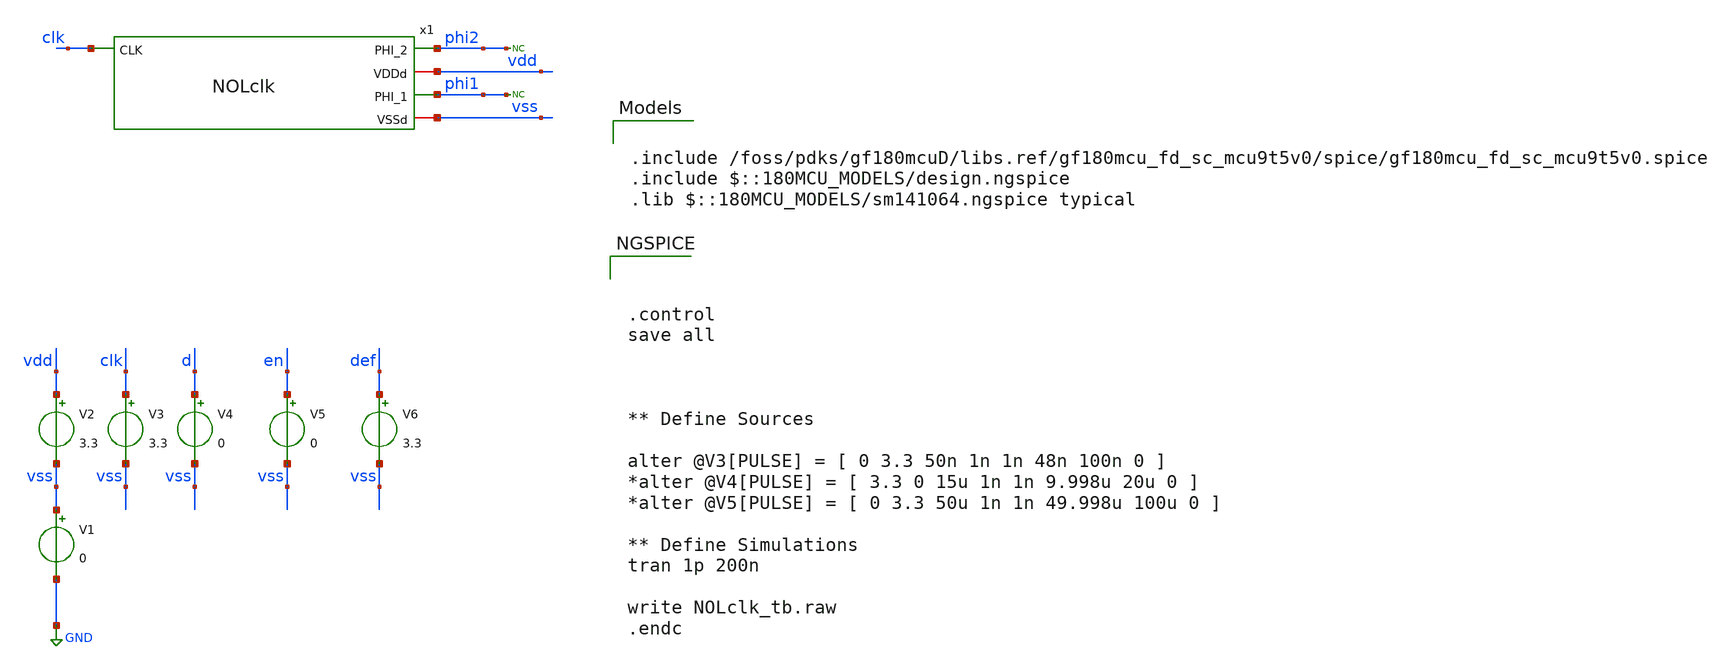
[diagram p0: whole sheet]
** sch_path: designs/libs/qw_tb_analog/NOLclk_tb/NOLclk_tb.sch
**.subckt NOLclk_tb
x1 phi2 clk vdd phi1 vss NOLclk
V1 vss GND 0
V2 vdd vss 3.3
V3 clk vss 3.3
V4 d vss 0
* noconn phi1
V5 en vss 0
V6 def vss 3.3
* noconn phi2
**** begin user architecture code

.include /foss/pdks/gf180mcuD/libs.ref/gf180mcu_fd_sc_mcu9t5v0/spice/gf180mcu_fd_sc_mcu9t5v0.spice
.include $::180MCU_MODELS/design.ngspice
.lib $::180MCU_MODELS/sm141064.ngspice typical




.control
save all



** Define Sources

alter @V3[PULSE] = [ 0 3.3 50n 1n 1n 48n 100n 0 ]
*alter @V4[PULSE] = [ 3.3 0 15u 1n 1n 9.998u 20u 0 ]
*alter @V5[PULSE] = [ 0 3.3 50u 1n 1n 49.998u 100u 0 ]

** Define Simulations
tran 1p 200n

write NOLclk_tb.raw
.endc


**** end user architecture code
**.ends

* expanding   symbol:  libs/qw_core_analog/NOLclk/NOLclk.sym # of pins=5
** sym_path: designs/libs/qw_core_analog/NOLclk/NOLclk.sym
** sch_path: designs/libs/qw_core_analog/NOLclk/NOLclk.sch
.subckt NOLclk PHI_2 CLK VDDd PHI_1 VSSd
*.ipin CLK
*.opin PHI_2
*.iopin VDDd
*.iopin VSSd
*.opin PHI_1
* noconn VDDd
* noconn VSSd
x21 CLK VSSd VDDd VSSd VDDd CLKB gf180mcu_fd_sc_mcu9t5v0__inv_1
x22 CLKB OUT_bot_d VSSd VDDd VSSd VDDd OUT_top gf180mcu_fd_sc_mcu9t5v0__nand2_1
x1 OUT_top_d CLKbuf VSSd VDDd VSSd VDDd OUT_bot gf180mcu_fd_sc_mcu9t5v0__nand2_1
x2 CLKB VSSd VDDd VSSd VDDd CLKbuf gf180mcu_fd_sc_mcu9t5v0__inv_1
x6 OUT_bot VSSd VDDd VSSd VDDd PHI_1 gf180mcu_fd_sc_mcu9t5v0__inv_1
x3 OUT_top VSSd VDDd VSSd VDDd PHI_2 gf180mcu_fd_sc_mcu9t5v0__inv_1
x4 VDDd PHI_2 net1 VSSd SmallW_Linv
x7 VDDd PHI_1 net2 VSSd SmallW_Linv
x12 VDDd net3 OUT_top_d VSSd SmallW_Linv_2
x14 VDDd net4 OUT_bot_d VSSd SmallW_Linv_2
x5 VDDd net1 net3 VSSd SmallW_Linv_2
x8 VDDd net2 net4 VSSd SmallW_Linv_2
.ends


* expanding   symbol:  libs/qw_core_analog/SmallW_Linv/SmallW_Linv.sym # of pins=4
** sym_path: designs/libs/qw_core_analog/SmallW_Linv/SmallW_Linv.sym
** sch_path: designs/libs/qw_core_analog/SmallW_Linv/SmallW_Linv.sch
.subckt SmallW_Linv vdd in out vss
*.iopin in
*.iopin out
*.iopin vdd
*.iopin vss
XM1 out in vss vss nfet_03v3 L=2u W=0.5u nf=1 ad='int((nf+1)/2) * W/nf * 0.18u' as='int((nf+2)/2) * W/nf * 0.18u'
+ pd='2*int((nf+1)/2) * (W/nf + 0.18u)' ps='2*int((nf+2)/2) * (W/nf + 0.18u)' nrd='0.18u / W' nrs='0.18u / W'
+ sa=0 sb=0 sd=0 m=1
XM2 out in vdd vdd pfet_03v3 L=2u W=1u nf=1 ad='int((nf+1)/2) * W/nf * 0.18u' as='int((nf+2)/2) * W/nf * 0.18u'
+ pd='2*int((nf+1)/2) * (W/nf + 0.18u)' ps='2*int((nf+2)/2) * (W/nf + 0.18u)' nrd='0.18u / W' nrs='0.18u / W'
+ sa=0 sb=0 sd=0 m=1
.ends


* expanding   symbol:  libs/qw_core_analog/SmallW_Linv_2/SmallW_Linv_2.sym # of pins=4
** sym_path: designs/libs/qw_core_analog/SmallW_Linv_2/SmallW_Linv_2.sym
** sch_path: designs/libs/qw_core_analog/SmallW_Linv_2/SmallW_Linv_2.sch
.subckt SmallW_Linv_2 vdd in out vss
*.iopin in
*.iopin out
*.iopin vdd
*.iopin vss
XM1 out in vss vss nfet_03v3 L=4u W=0.5u nf=1 ad='int((nf+1)/2) * W/nf * 0.18u' as='int((nf+2)/2) * W/nf * 0.18u'
+ pd='2*int((nf+1)/2) * (W/nf + 0.18u)' ps='2*int((nf+2)/2) * (W/nf + 0.18u)' nrd='0.18u / W' nrs='0.18u / W'
+ sa=0 sb=0 sd=0 m=1
XM2 out in vdd vdd pfet_03v3 L=4u W=1u nf=1 ad='int((nf+1)/2) * W/nf * 0.18u' as='int((nf+2)/2) * W/nf * 0.18u'
+ pd='2*int((nf+1)/2) * (W/nf + 0.18u)' ps='2*int((nf+2)/2) * (W/nf + 0.18u)' nrd='0.18u / W' nrs='0.18u / W'
+ sa=0 sb=0 sd=0 m=1
.ends

.GLOBAL GND
.end
